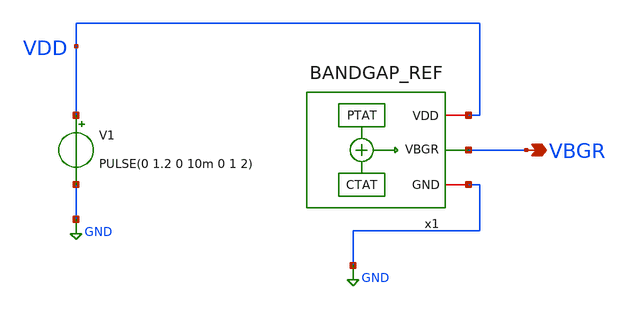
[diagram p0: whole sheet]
** sch_path: xschem/bgr/tb_BGR_PEX.sch
**.subckt tb_BGR_PEX VBGR
*.opin VBGR
V1 VDD GND PULSE(0 1.2 0 10m 0 1 2)
x1 VDD GND VBGR BANDGAP_REF_PEX
**** begin user architecture code



.option rshunt=1.0e12
.control
save all
save VDD
alter V1 dc 1.2

op
print I(Vmeas)

dc TEMP 100 -50 -5
print I(Vmeas)

write tb_BGR_PEX_temp.raw
.endc

.control
save all
tran 100u 15m

print I(Vmeas)

write tb_BGR_PEX_transient.raw
.endc




.include /foss/designs/unicasss-tools/SG13G2_2.4GHz_LC_VCO_FPLL/pex/BANDGAP_REF__BANDGAP_REF/magic_RC/BANDGAP_REF.pex.spice
.lib cornerMOSlv.lib mos_tt
.lib cornerMOShv.lib mos_tt
.lib cornerRES.lib res_typ
.lib cornerCAP.lib cap_typ

**** end user architecture code
**.ends
.GLOBAL GND
.end
